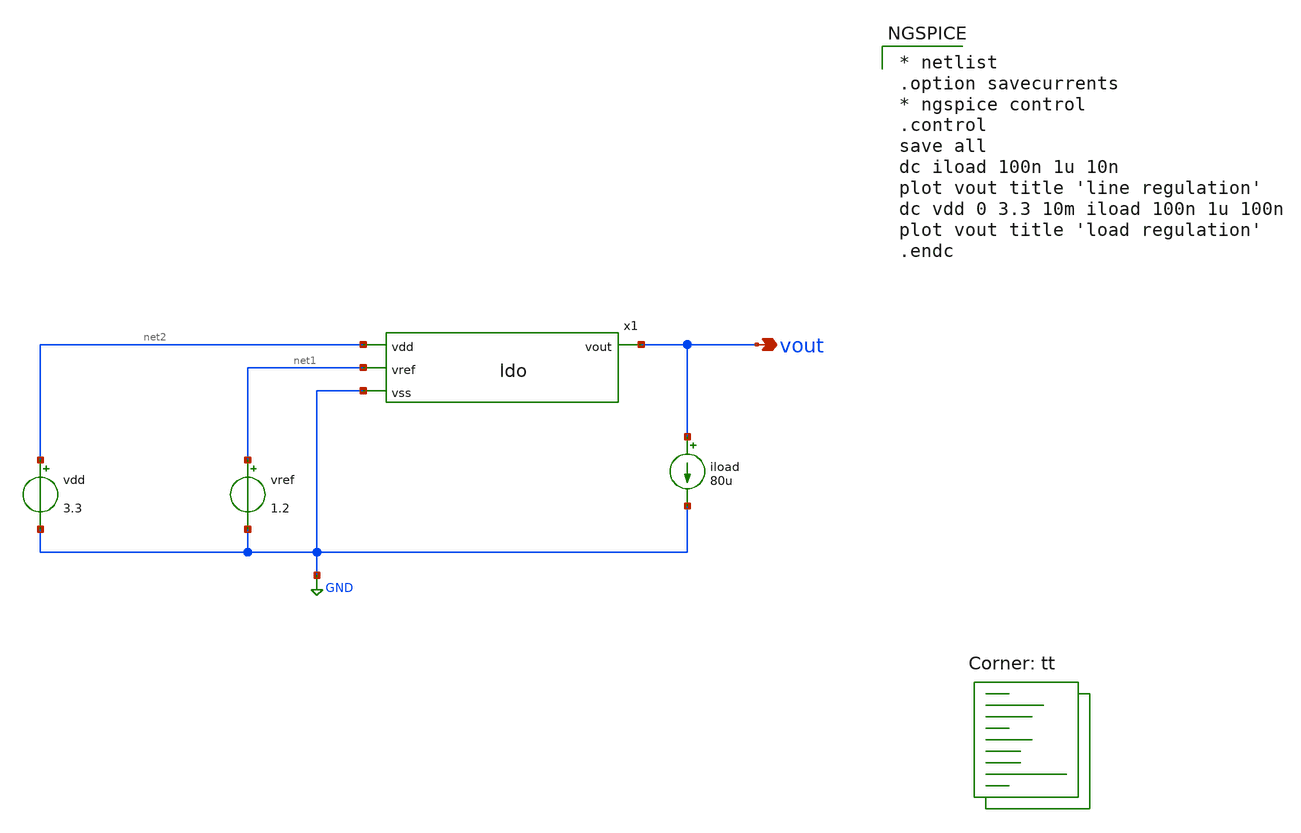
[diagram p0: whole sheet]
** sch_path: xschem/ldo_regulation_tb.sch
**.subckt ldo_regulation_tb vout
*.opin vout
x1 net2 net1 GND vout ldo
vref net1 GND 1.2
vdd net2 GND 3.3
iload vout GND 80u
**** begin user architecture code
.lib $::SKYWATER_MODELS/sky130.lib.spice tt

* netlist
.option savecurrents
* ngspice control
.control
save all
dc iload 100n 1u 10n
plot vout title 'line regulation'
dc vdd 0 3.3 10m iload 100n 1u 100n
plot vout title 'load regulation'
.endc


**** end user architecture code
**.ends

* expanding   symbol:  ldo.sym # of pins=4
** sym_path: xschem/ldo.sym
** sch_path: xschem/ldo.sch
.subckt ldo vdd vref vss vout
*.ipin vdd
*.ipin vref
*.ipin vss
*.opin vout
XM1 net1 net4 vdd vdd sky130_fd_pr__pfet_g5v0d10v5 L=1 W=6 nf=1 ad='int((nf+1)/2) * W/nf * 0.29' as='int((nf+2)/2) * W/nf * 0.29'
+ pd='2*int((nf+1)/2) * (W/nf + 0.29)' ps='2*int((nf+2)/2) * (W/nf + 0.29)' nrd='0.29 / W' nrs='0.29 / W'
+ sa=0 sb=0 sd=0 mult=1 m=1
XM2 vp vbp net1 vdd sky130_fd_pr__pfet_g5v0d10v5 L=1 W=6 nf=1 ad='int((nf+1)/2) * W/nf * 0.29' as='int((nf+2)/2) * W/nf * 0.29'
+ pd='2*int((nf+1)/2) * (W/nf + 0.29)' ps='2*int((nf+2)/2) * (W/nf + 0.29)' nrd='0.29 / W' nrs='0.29 / W'
+ sa=0 sb=0 sd=0 mult=1 m=1
XM3 vout_p vctrl vp vdd sky130_fd_pr__pfet_g5v0d10v5 L=2 W=3 nf=1 ad='int((nf+1)/2) * W/nf * 0.29' as='int((nf+2)/2) * W/nf * 0.29'
+ pd='2*int((nf+1)/2) * (W/nf + 0.29)' ps='2*int((nf+2)/2) * (W/nf + 0.29)' nrd='0.29 / W' nrs='0.29 / W'
+ sa=0 sb=0 sd=0 mult=1 m=1
XM4 vref_p vref vp vdd sky130_fd_pr__pfet_g5v0d10v5 L=2 W=3 nf=1 ad='int((nf+1)/2) * W/nf * 0.29' as='int((nf+2)/2) * W/nf * 0.29'
+ pd='2*int((nf+1)/2) * (W/nf + 0.29)' ps='2*int((nf+2)/2) * (W/nf + 0.29)' nrd='0.29 / W' nrs='0.29 / W'
+ sa=0 sb=0 sd=0 mult=1 m=1
XM5 net3 net2 vdd vdd sky130_fd_pr__pfet_g5v0d10v5 L=1 W=10 nf=1 ad='int((nf+1)/2) * W/nf * 0.29' as='int((nf+2)/2) * W/nf * 0.29'
+ pd='2*int((nf+1)/2) * (W/nf + 0.29)' ps='2*int((nf+2)/2) * (W/nf + 0.29)' nrd='0.29 / W' nrs='0.29 / W'
+ sa=0 sb=0 sd=0 mult=1 m=1
XM6 vy net2 vdd vdd sky130_fd_pr__pfet_g5v0d10v5 L=1 W=10 nf=1 ad='int((nf+1)/2) * W/nf * 0.29' as='int((nf+2)/2) * W/nf * 0.29'
+ pd='2*int((nf+1)/2) * (W/nf + 0.29)' ps='2*int((nf+2)/2) * (W/nf + 0.29)' nrd='0.29 / W' nrs='0.29 / W'
+ sa=0 sb=0 sd=0 mult=1 m=1
XM7 net2 vb2 net3 vdd sky130_fd_pr__pfet_g5v0d10v5 L=1 W=10 nf=1 ad='int((nf+1)/2) * W/nf * 0.29' as='int((nf+2)/2) * W/nf * 0.29'
+ pd='2*int((nf+1)/2) * (W/nf + 0.29)' ps='2*int((nf+2)/2) * (W/nf + 0.29)' nrd='0.29 / W' nrs='0.29 / W'
+ sa=0 sb=0 sd=0 mult=1 m=1
XM8 vx vb2 vy vdd sky130_fd_pr__pfet_g5v0d10v5 L=1 W=10 nf=1 ad='int((nf+1)/2) * W/nf * 0.29' as='int((nf+2)/2) * W/nf * 0.29'
+ pd='2*int((nf+1)/2) * (W/nf + 0.29)' ps='2*int((nf+2)/2) * (W/nf + 0.29)' nrd='0.29 / W' nrs='0.29 / W'
+ sa=0 sb=0 sd=0 mult=1 m=1
XM9 net2 vb1 vref_p vss sky130_fd_pr__nfet_g5v0d10v5 L=1 W=2 nf=1 ad='int((nf+1)/2) * W/nf * 0.29' as='int((nf+2)/2) * W/nf * 0.29'
+ pd='2*int((nf+1)/2) * (W/nf + 0.29)' ps='2*int((nf+2)/2) * (W/nf + 0.29)' nrd='0.29 / W' nrs='0.29 / W'
+ sa=0 sb=0 sd=0 mult=1 m=1
XM10 vx vb1 vout_p vss sky130_fd_pr__nfet_g5v0d10v5 L=1 W=2 nf=1 ad='int((nf+1)/2) * W/nf * 0.29' as='int((nf+2)/2) * W/nf * 0.29'
+ pd='2*int((nf+1)/2) * (W/nf + 0.29)' ps='2*int((nf+2)/2) * (W/nf + 0.29)' nrd='0.29 / W' nrs='0.29 / W'
+ sa=0 sb=0 sd=0 mult=1 m=1
XM11 vref_p vbn vss vss sky130_fd_pr__nfet_g5v0d10v5 L=3 W=7 nf=1 ad='int((nf+1)/2) * W/nf * 0.29' as='int((nf+2)/2) * W/nf * 0.29'
+ pd='2*int((nf+1)/2) * (W/nf + 0.29)' ps='2*int((nf+2)/2) * (W/nf + 0.29)' nrd='0.29 / W' nrs='0.29 / W'
+ sa=0 sb=0 sd=0 mult=1 m=1
XM12 vout_p vbn vss vss sky130_fd_pr__nfet_g5v0d10v5 L=3 W=7 nf=1 ad='int((nf+1)/2) * W/nf * 0.29' as='int((nf+2)/2) * W/nf * 0.29'
+ pd='2*int((nf+1)/2) * (W/nf + 0.29)' ps='2*int((nf+2)/2) * (W/nf + 0.29)' nrd='0.29 / W' nrs='0.29 / W'
+ sa=0 sb=0 sd=0 mult=1 m=1
XM13 vdd vx vout vss sky130_fd_pr__nfet_g5v0d10v5 L=0.5 W=100 nf=1 ad='int((nf+1)/2) * W/nf * 0.29' as='int((nf+2)/2) * W/nf * 0.29'
+ pd='2*int((nf+1)/2) * (W/nf + 0.29)' ps='2*int((nf+2)/2) * (W/nf + 0.29)' nrd='0.29 / W' nrs='0.29 / W'
+ sa=0 sb=0 sd=0 mult=1 m=1
R1 vout vctrl 1e6 m=1
R2 vctrl vss 2e6 m=1
XM14 net5 net4 vdd vdd sky130_fd_pr__pfet_g5v0d10v5 L=1 W=6 nf=1 ad='int((nf+1)/2) * W/nf * 0.29' as='int((nf+2)/2) * W/nf * 0.29'
+ pd='2*int((nf+1)/2) * (W/nf + 0.29)' ps='2*int((nf+2)/2) * (W/nf + 0.29)' nrd='0.29 / W' nrs='0.29 / W'
+ sa=0 sb=0 sd=0 mult=1 m=1
XM15 net4 vbp net5 vdd sky130_fd_pr__pfet_g5v0d10v5 L=1 W=6 nf=1 ad='int((nf+1)/2) * W/nf * 0.29' as='int((nf+2)/2) * W/nf * 0.29'
+ pd='2*int((nf+1)/2) * (W/nf + 0.29)' ps='2*int((nf+2)/2) * (W/nf + 0.29)' nrd='0.29 / W' nrs='0.29 / W'
+ sa=0 sb=0 sd=0 mult=1 m=1
I0 net4 vss 600n
XM16 vbn vbn vss vss sky130_fd_pr__nfet_g5v0d10v5 L=3 W=7 nf=1 ad='int((nf+1)/2) * W/nf * 0.29' as='int((nf+2)/2) * W/nf * 0.29'
+ pd='2*int((nf+1)/2) * (W/nf + 0.29)' ps='2*int((nf+2)/2) * (W/nf + 0.29)' nrd='0.29 / W' nrs='0.29 / W'
+ sa=0 sb=0 sd=0 mult=1 m=1
I1 vdd vbn 700n
V1 vb1 vss 2
V2 vb2 vss 1.9
V3 vbp vss 1.5
.ends

.GLOBAL GND
.end
